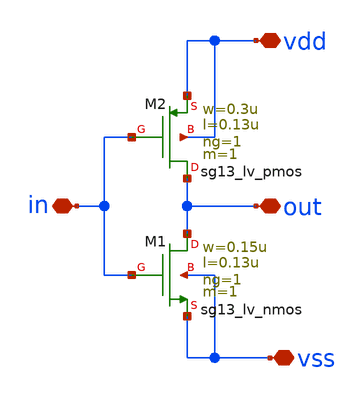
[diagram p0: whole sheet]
** sch_path: BinarytoThermo/inv.sch
**.subckt inv in out vdd vss
*.iopin in
*.iopin out
*.iopin vdd
*.iopin vss
XM1 out in vss vss sg13_lv_nmos w=0.15u l=0.13u ng=1 m=1 mm_ok=1
XM2 out in vdd vdd sg13_lv_pmos w=0.3u l=0.13u ng=1 m=1 mm_ok=1
**.ends
.end
